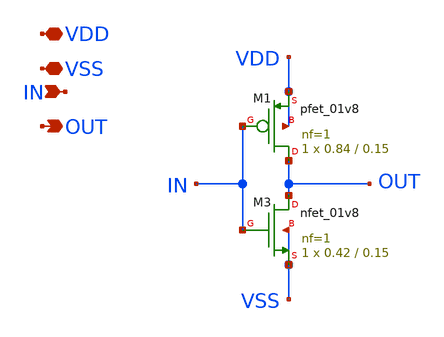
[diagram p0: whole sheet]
** sch_path: Xschem/PLL_TOP_Schematics/PFD_INV.sch
**.subckt PFD_INV VDD VSS IN OUT
*.iopin VDD
*.iopin VSS
*.ipin IN
*.opin OUT
XM1 OUT IN VDD VDD sky130_fd_pr__pfet_01v8 L=0.15 W=0.84 nf=1 ad='int((nf+1)/2) * W/nf * 0.29' as='int((nf+2)/2) * W/nf * 0.29'
+ pd='2*int((nf+1)/2) * (W/nf + 0.29)' ps='2*int((nf+2)/2) * (W/nf + 0.29)' nrd='0.29 / W' nrs='0.29 / W'
+ sa=0 sb=0 sd=0 mult=1 m=1
XM3 OUT IN VSS VSS sky130_fd_pr__nfet_01v8 L=0.15 W=0.42 nf=1 ad='int((nf+1)/2) * W/nf * 0.29' as='int((nf+2)/2) * W/nf * 0.29'
+ pd='2*int((nf+1)/2) * (W/nf + 0.29)' ps='2*int((nf+2)/2) * (W/nf + 0.29)' nrd='0.29 / W' nrs='0.29 / W'
+ sa=0 sb=0 sd=0 mult=1 m=1
**.ends
.end
